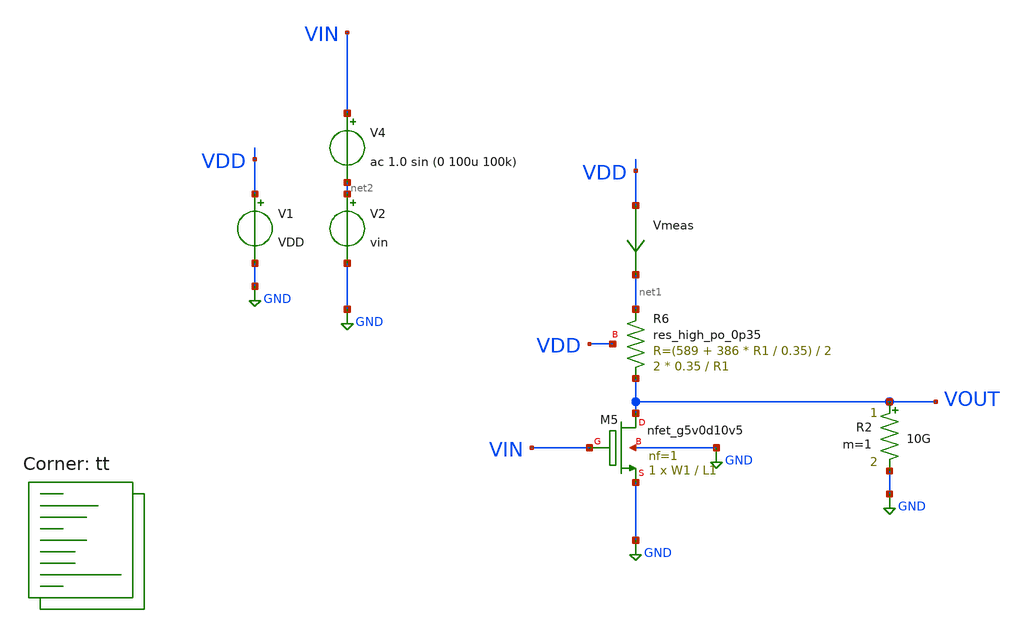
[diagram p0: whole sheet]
** sch_path: amplifiers/single_stage_amps/basic_stages/cs_resistor_stage/genetic_automatic/cs_resistor_stage_test.sch
**.subckt cs_resistor_stage_test
Vmeas VDD net1 0
.save i(vmeas)
V1 VDD GND VDD
V2 net2 GND vin
R2 VOUT GND 10G m=1
XR6 VOUT net1 VDD sky130_fd_pr__res_high_po_0p35 L=R1 mult=2 m=2
V4 VIN net2 ac 1.0 sin (0 100u 100k)
XM5 VOUT VIN GND GND sky130_fd_pr__nfet_g5v0d10v5 L=L1 W=W1 nf=1 ad='int((1 + 1)/2) * W1 / 1 * 0.29'
+ as='int((1 + 2)/2) * W1 / 1 * 0.29' pd='2*int((1 + 1)/2) * (W1 / 1 + 0.29)' ps='2*int((1 + 2)/2) * (W1 / 1 + 0.29)'
+ nrd='0.29 / W1 ' nrs='0.29 / W1 ' sa=0 sb=0 sd=0 mult=1 m=1
**** begin user architecture code

**************************************************************
**************************************************************
**************************************************************
**************************************************************
**************************************************************
*LIBs*********************************************************
**************************************************************
**************************************************************
**************************************************************
**************************************************************
**************************************************************
*.lib $::SKYWATER_MODELS/sky130.lib.spice tt
* chose the corners in the corner file
* tt_mm for mismatch
* ss ff sf fs standart corners
* ll hh lh hl capacitor and resistors corners
* mc for total process variation including corners
**************************************************************
**************************************************************
**************************************************************
**************************************************************
**************************************************************
*Corners/montecarlo options***********************************
**************************************************************
**************************************************************
**************************************************************
**************************************************************
**************************************************************
.TEMP 27
**************************************************************
**************************************************************
**************************************************************
**************************************************************
*SIMULATION and Plots*****************************************
**************************************************************
**************************************************************
**************************************************************
**************************************************************


.control
.param R1 = 5
.param L1 = 0.5
.param VDD = 5
.param W1 = 50
.param vin =  2



save all
dc V2 0 5 0.01
plot v(VOUT) deriv(v(VOUT))



.endc

.lib $::SKYWATER_MODELS/sky130.lib.spice tt
**** end user architecture code
**.ends
.GLOBAL GND
.end
